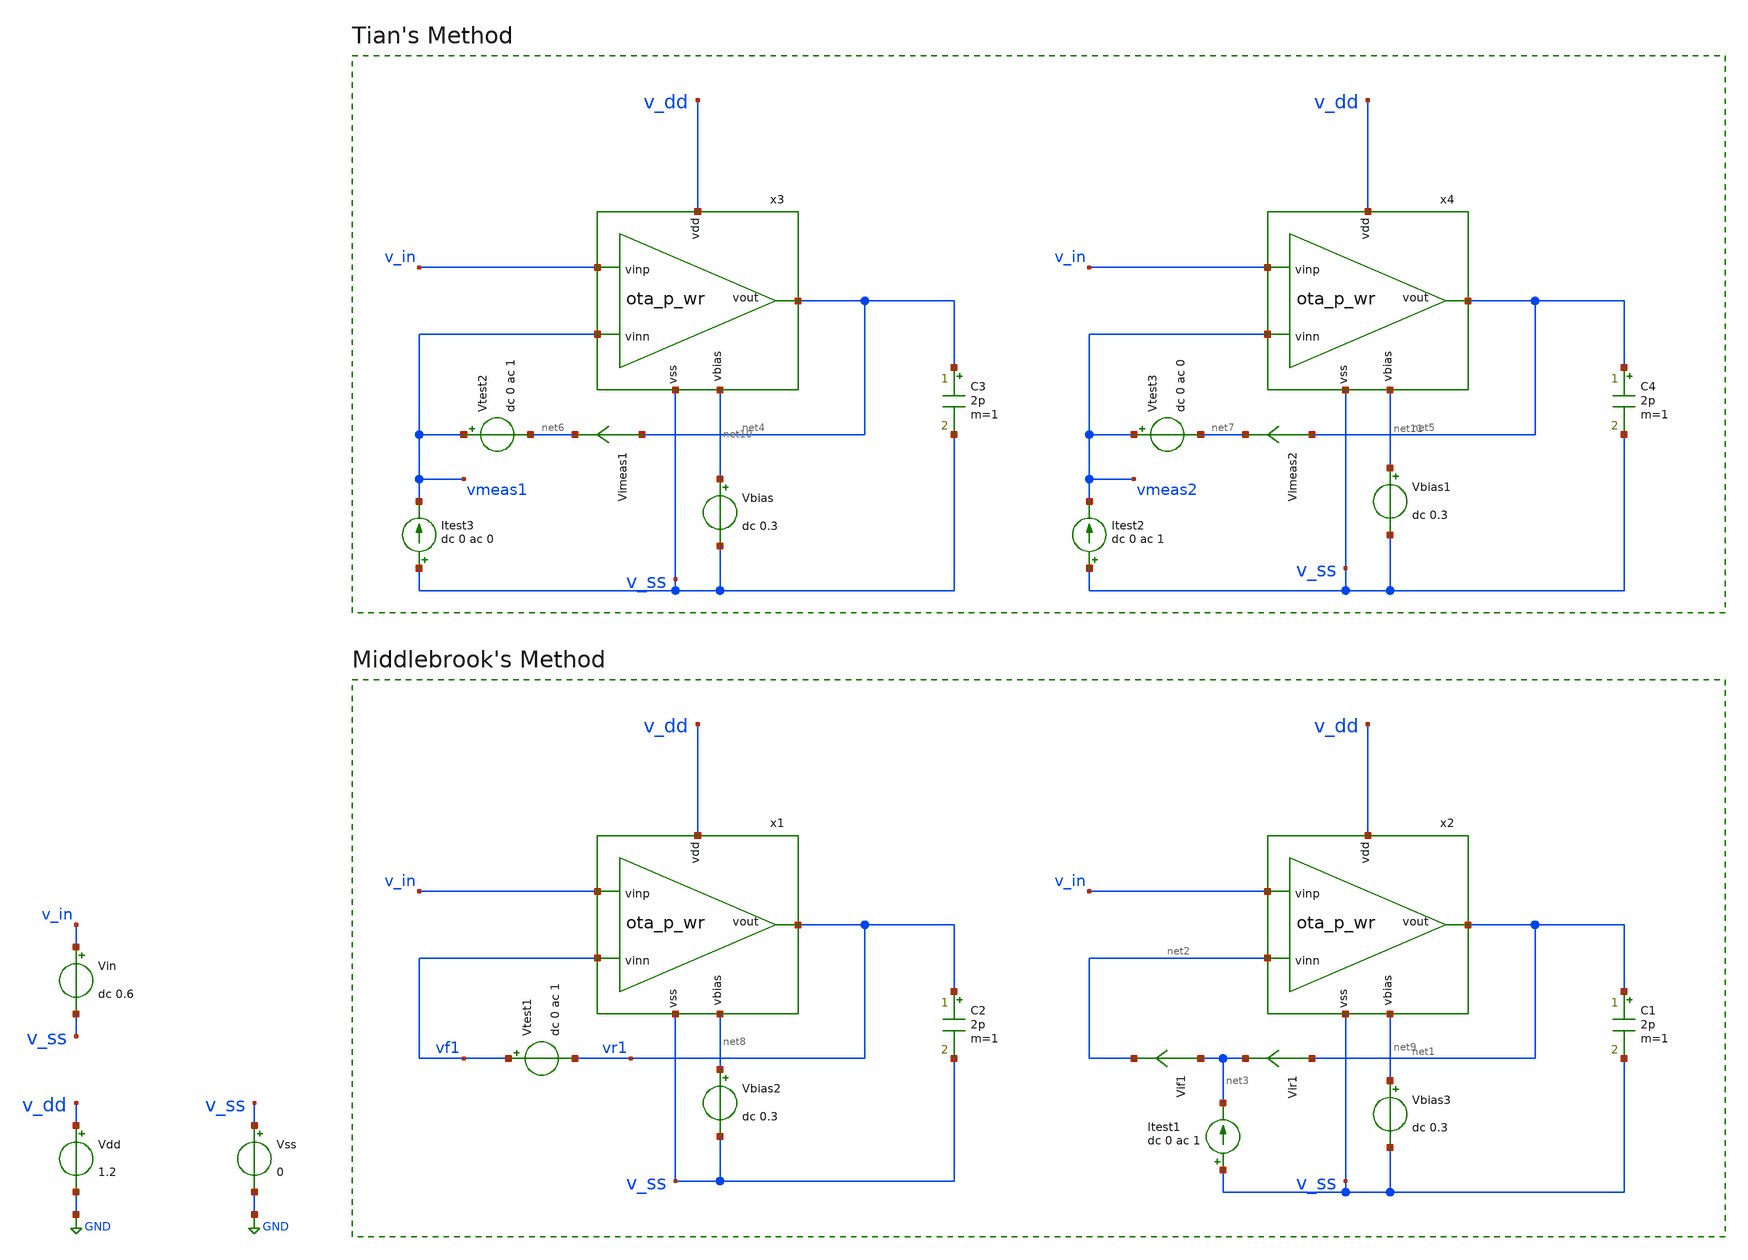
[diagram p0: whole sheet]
** sch_path: v2_feature_extr_withf/ota_p-wr_tb-loopgain.sch
* (c) 2024-2025 H. Pretl, S. Dorrer, Apache-2.0 license
**.subckt ota_p-wr_tb-loopgain
Vdd v_dd GND 1.2
Vss v_ss GND 0
Vin v_in v_ss dc 0.6
C2 vr1 v_ss 2p m=1
x1 v_dd vr1 v_in vf1 net8 v_ss ota_p_wr
Vtest1 vf1 vr1 dc 0 ac 1
C1 net1 v_ss 2p m=1
x2 v_dd net1 v_in net2 net9 v_ss ota_p_wr
Vir1 net1 net3 0
.save i(vir1)
Vif1 net3 net2 0
.save i(vif1)
Itest1 v_ss net3 dc 0 ac 1
C3 net4 v_ss 2p m=1
x3 v_dd net4 v_in vmeas1 net10 v_ss ota_p_wr
C4 net5 v_ss 2p m=1
x4 v_dd net5 v_in vmeas2 net11 v_ss ota_p_wr
Itest3 v_ss vmeas1 dc 0 ac 0
Vtest2 vmeas1 net6 dc 0 ac 1
Vimeas1 net4 net6 0
.save i(vimeas1)
Itest2 v_ss vmeas2 dc 0 ac 1
Vtest3 vmeas2 net7 dc 0 ac 0
Vimeas2 net5 net7 0
.save i(vimeas2)
Vbias net10 v_ss dc 0.3
Vbias1 net11 v_ss dc 0.3
Vbias2 net8 v_ss dc 0.3
Vbias3 net9 v_ss dc 0.3
**** begin user architecture code
 .lib cornerMOSlv.lib mos_tt



.param temp=27
.options savecurrents reltol=1e-3 abstol=1e-12 gmin=1e-15
.control
save all

* Operating Point Analysis
op
remzerovec
write ota_p-wr_tb-loopgain.raw
set appendwrite

* AC Analysis
ac dec 101 1 100G
remzerovec
write ota_p-wr_tb-loopgain.raw
set appendwrite

* Middlebrook's Method
let tv=-v(vr1)/v(vf1)
let ti=-i(vir1)/i(vif1)
let tmb=(tv*ti - 1)/(tv + ti + 2)

*plot db(tmb) ylabel 'Magnitude - Middlebrook'
*plot 180/pi*cphase(tmb) ylabel 'Phase - Middlebrook'

* Tian's Method
* vtest=0, itest=1:
let A=i(Vimeas2)
let C=v(vmeas2)

* vtest=1, itest=0:
let B=i(Vimeas1)
let D=v(vmeas1)
let ttian=(A*D-B*C-A)/(2*(B*C-A*D)+A-D+1)

*plot db(ttian) ylabel 'Magnitude - Tian'
*plot 180/pi*cphase(ttian) ylabel 'Phase - Tian'

* Middlebrook vs. Tian
plot db(tmb) db(ttian) ylabel 'Magnitude'
plot 180/pi*cphase(tmb) 180/pi*cphase(ttian) ylabel 'Phase'

write ota_p-wr_tb-loopgain.raw

*quit
.endc


**** end user architecture code
**.ends
.GLOBAL GND
.end
